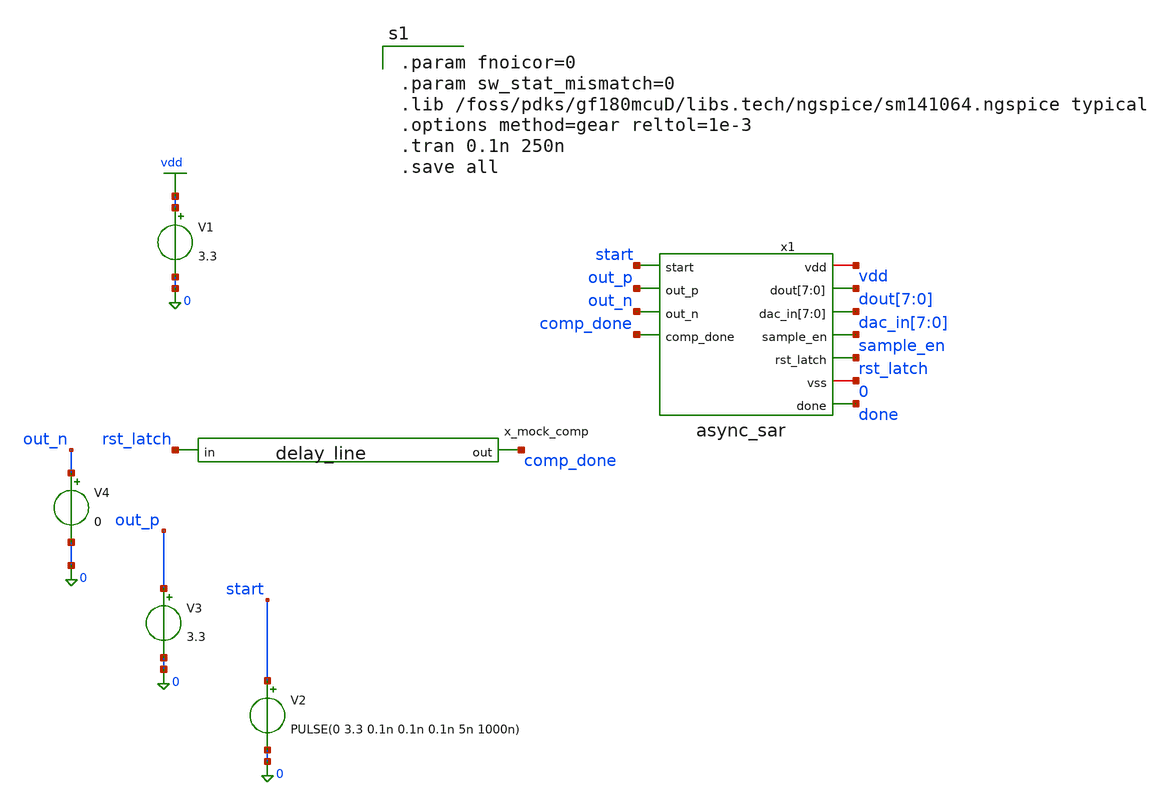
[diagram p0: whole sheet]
** sch_path: xschem/sar_adc/blocks/async_sar/testbench/tb_async_sar.sch
**.subckt tb_async_sar
V1 vdd 0 3.3
V2 start 0 PULSE(0 3.3 0.1n 0.1n 0.1n 5n 1000n)
V3 out_p 0 3.3
x_mock_comp comp_done rst_latch delay_line
x1 sample_en rst_latch done dout[7] dout[6] dout[5] dout[4] dout[3] dout[2] dout[1] dout[0] start
+ dac_in[7] dac_in[6] dac_in[5] dac_in[4] dac_in[3] dac_in[2] dac_in[1] dac_in[0] out_p out_n vdd comp_done 0
+ async_sar
V4 out_n 0 0
**** begin user architecture code

.param fnoicor=0
.param sw_stat_mismatch=0
.lib /foss/pdks/gf180mcuD/libs.tech/ngspice/sm141064.ngspice typical
.options method=gear reltol=1e-3
.tran 0.1n 250n
.save all

**** end user architecture code
**.ends
.GLOBAL vdd
.end
